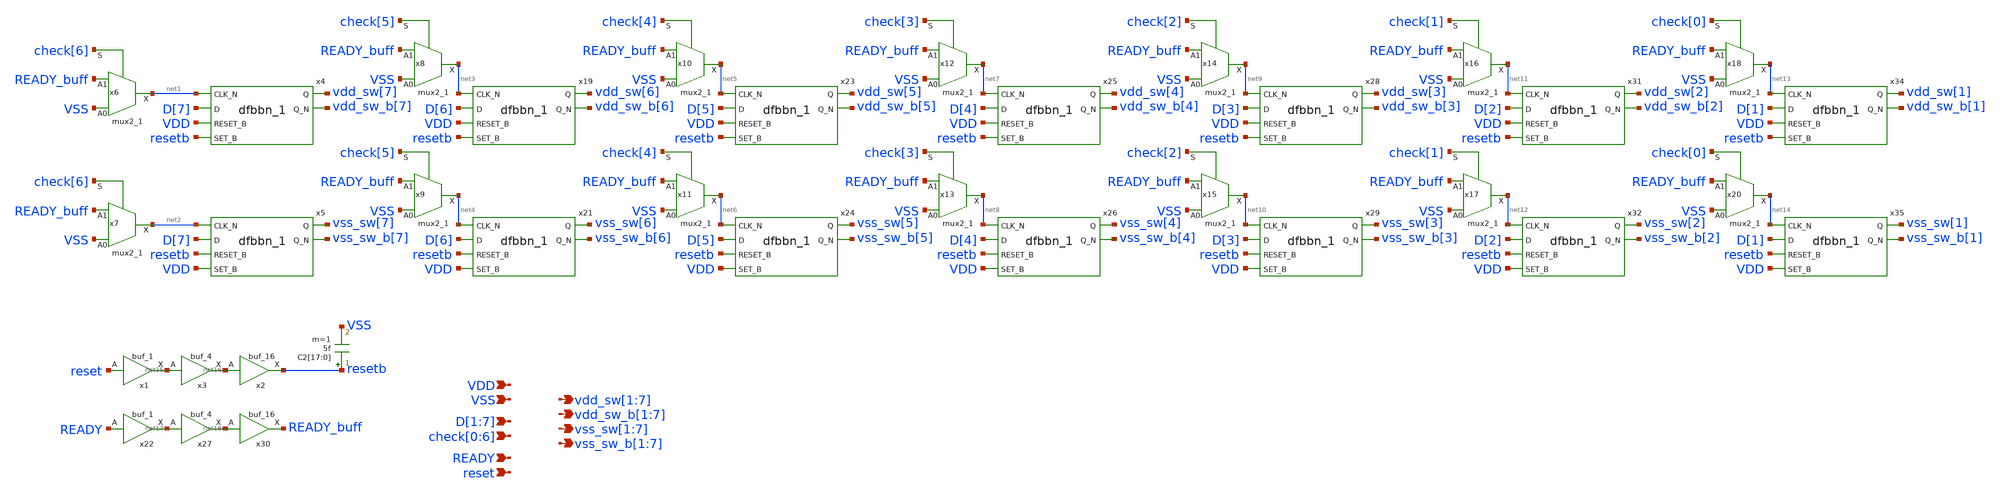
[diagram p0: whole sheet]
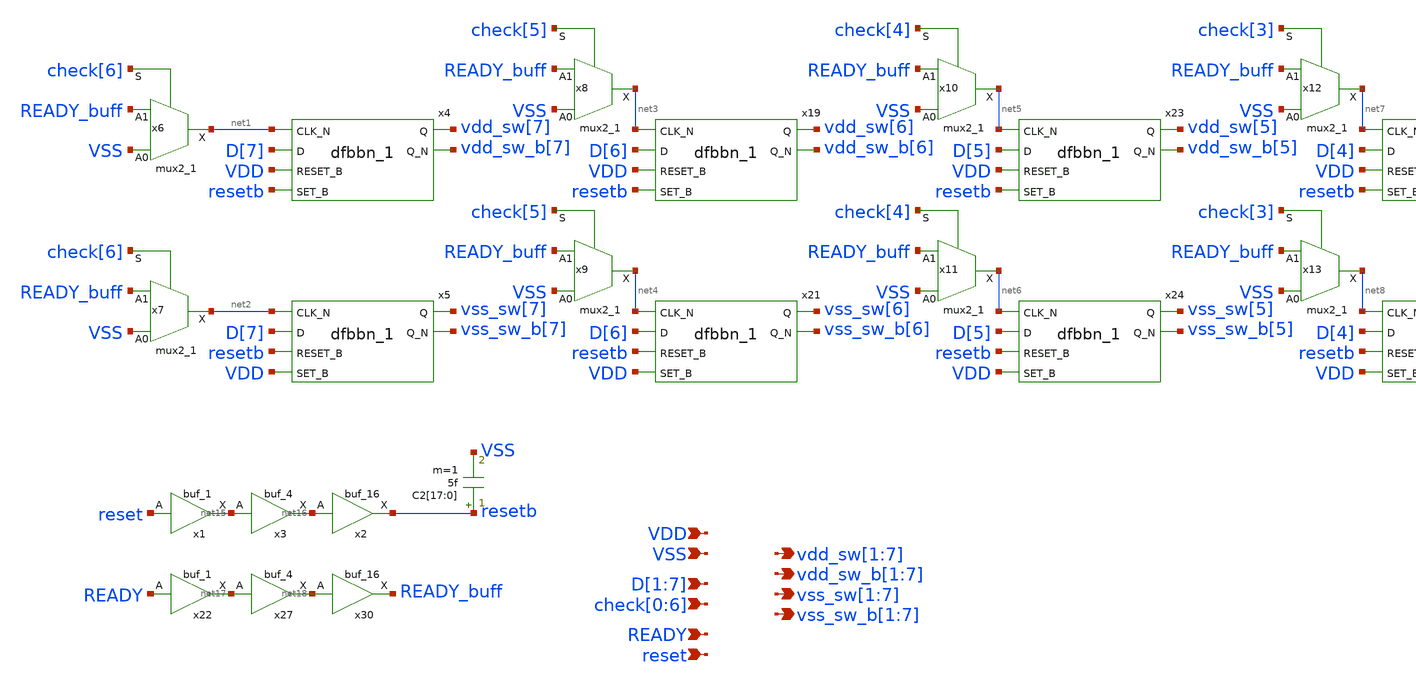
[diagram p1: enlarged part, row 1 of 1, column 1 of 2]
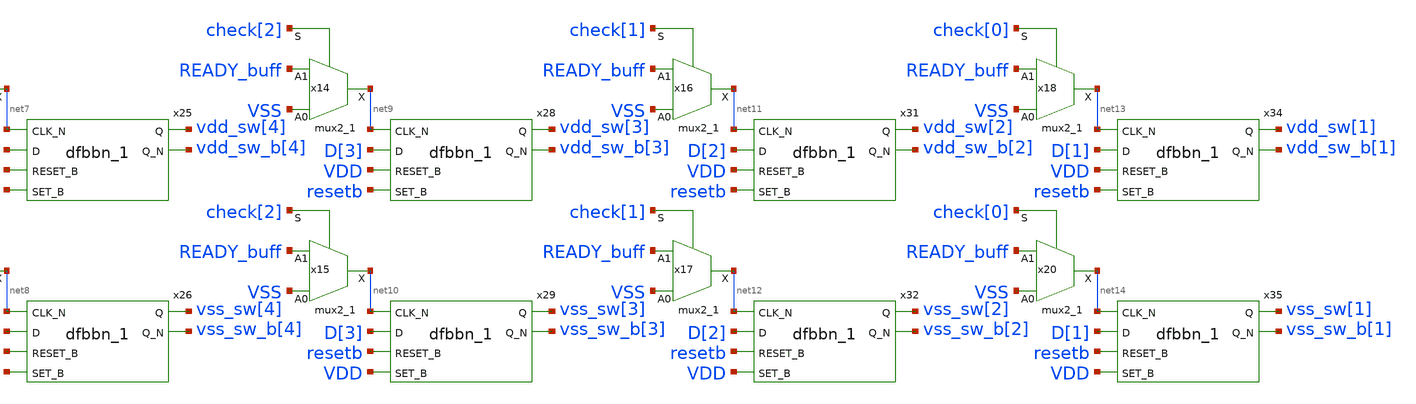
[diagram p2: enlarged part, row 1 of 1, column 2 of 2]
** sch_path: hgu/xschem/hgu_sarlogic_sw_ctrl.sch
**.subckt hgu_sarlogic_sw_ctrl vdd_sw[1],vdd_sw[2],vdd_sw[3],vdd_sw[4],vdd_sw[5],vdd_sw[6],vdd_sw[7]
*+ vdd_sw_b[1],vdd_sw_b[2],vdd_sw_b[3],vdd_sw_b[4],vdd_sw_b[5],vdd_sw_b[6],vdd_sw_b[7] vss_sw[1],vss_sw[2],vss_sw[3],vss_sw[4],vss_sw[5],vss_sw[6],vss_sw[7]
*+ vss_sw_b[1],vss_sw_b[2],vss_sw_b[3],vss_sw_b[4],vss_sw_b[5],vss_sw_b[6],vss_sw_b[7] VDD VSS READY D[1],D[2],D[3],D[4],D[5],D[6],D[7]
*+ check[0],check[1],check[2],check[3],check[4],check[5],check[6] reset
*.opin vdd_sw[1],vdd_sw[2],vdd_sw[3],vdd_sw[4],vdd_sw[5],vdd_sw[6],vdd_sw[7]
*.opin vdd_sw_b[1],vdd_sw_b[2],vdd_sw_b[3],vdd_sw_b[4],vdd_sw_b[5],vdd_sw_b[6],vdd_sw_b[7]
*.opin vss_sw[1],vss_sw[2],vss_sw[3],vss_sw[4],vss_sw[5],vss_sw[6],vss_sw[7]
*.opin vss_sw_b[1],vss_sw_b[2],vss_sw_b[3],vss_sw_b[4],vss_sw_b[5],vss_sw_b[6],vss_sw_b[7]
*.ipin VDD
*.ipin VSS
*.ipin READY
*.ipin D[1],D[2],D[3],D[4],D[5],D[6],D[7]
*.ipin check[0],check[1],check[2],check[3],check[4],check[5],check[6]
*.ipin reset
x4 net1 D[7] VDD resetb VSS VSS VDD VDD vdd_sw[7] vdd_sw_b[7] sky130_fd_sc_hd__dfbbn_1
x5 net2 D[7] resetb VDD VSS VSS VDD VDD vss_sw[7] vss_sw_b[7] sky130_fd_sc_hd__dfbbn_1
x19 net3 D[6] VDD resetb VSS VSS VDD VDD vdd_sw[6] vdd_sw_b[6] sky130_fd_sc_hd__dfbbn_1
x21 net4 D[6] resetb VDD VSS VSS VDD VDD vss_sw[6] vss_sw_b[6] sky130_fd_sc_hd__dfbbn_1
x23 net5 D[5] VDD resetb VSS VSS VDD VDD vdd_sw[5] vdd_sw_b[5] sky130_fd_sc_hd__dfbbn_1
x24 net6 D[5] resetb VDD VSS VSS VDD VDD vss_sw[5] vss_sw_b[5] sky130_fd_sc_hd__dfbbn_1
x25 net7 D[4] VDD resetb VSS VSS VDD VDD vdd_sw[4] vdd_sw_b[4] sky130_fd_sc_hd__dfbbn_1
x26 net8 D[4] resetb VDD VSS VSS VDD VDD vss_sw[4] vss_sw_b[4] sky130_fd_sc_hd__dfbbn_1
x28 net9 D[3] VDD resetb VSS VSS VDD VDD vdd_sw[3] vdd_sw_b[3] sky130_fd_sc_hd__dfbbn_1
x29 net10 D[3] resetb VDD VSS VSS VDD VDD vss_sw[3] vss_sw_b[3] sky130_fd_sc_hd__dfbbn_1
x31 net11 D[2] VDD resetb VSS VSS VDD VDD vdd_sw[2] vdd_sw_b[2] sky130_fd_sc_hd__dfbbn_1
x32 net12 D[2] resetb VDD VSS VSS VDD VDD vss_sw[2] vss_sw_b[2] sky130_fd_sc_hd__dfbbn_1
x34 net13 D[1] VDD resetb VSS VSS VDD VDD vdd_sw[1] vdd_sw_b[1] sky130_fd_sc_hd__dfbbn_1
x35 net14 D[1] resetb VDD VSS VSS VDD VDD vss_sw[1] vss_sw_b[1] sky130_fd_sc_hd__dfbbn_1
x6 VSS READY_buff check[6] VSS VSS VDD VDD net1 sky130_fd_sc_hd__mux2_1
x7 VSS READY_buff check[6] VSS VSS VDD VDD net2 sky130_fd_sc_hd__mux2_1
x8 VSS READY_buff check[5] VSS VSS VDD VDD net3 sky130_fd_sc_hd__mux2_1
x9 VSS READY_buff check[5] VSS VSS VDD VDD net4 sky130_fd_sc_hd__mux2_1
x10 VSS READY_buff check[4] VSS VSS VDD VDD net5 sky130_fd_sc_hd__mux2_1
x11 VSS READY_buff check[4] VSS VSS VDD VDD net6 sky130_fd_sc_hd__mux2_1
x12 VSS READY_buff check[3] VSS VSS VDD VDD net7 sky130_fd_sc_hd__mux2_1
x13 VSS READY_buff check[3] VSS VSS VDD VDD net8 sky130_fd_sc_hd__mux2_1
x14 VSS READY_buff check[2] VSS VSS VDD VDD net9 sky130_fd_sc_hd__mux2_1
x15 VSS READY_buff check[2] VSS VSS VDD VDD net10 sky130_fd_sc_hd__mux2_1
x16 VSS READY_buff check[1] VSS VSS VDD VDD net11 sky130_fd_sc_hd__mux2_1
x17 VSS READY_buff check[1] VSS VSS VDD VDD net12 sky130_fd_sc_hd__mux2_1
x18 VSS READY_buff check[0] VSS VSS VDD VDD net13 sky130_fd_sc_hd__mux2_1
x20 VSS READY_buff check[0] VSS VSS VDD VDD net14 sky130_fd_sc_hd__mux2_1
C2[17] resetb VSS 5f m=1
C2[16] resetb VSS 5f m=1
C2[15] resetb VSS 5f m=1
C2[14] resetb VSS 5f m=1
C2[13] resetb VSS 5f m=1
C2[12] resetb VSS 5f m=1
C2[11] resetb VSS 5f m=1
C2[10] resetb VSS 5f m=1
C2[9] resetb VSS 5f m=1
C2[8] resetb VSS 5f m=1
C2[7] resetb VSS 5f m=1
C2[6] resetb VSS 5f m=1
C2[5] resetb VSS 5f m=1
C2[4] resetb VSS 5f m=1
C2[3] resetb VSS 5f m=1
C2[2] resetb VSS 5f m=1
C2[1] resetb VSS 5f m=1
C2[0] resetb VSS 5f m=1
x1 reset VSS VSS VDD VDD net15 sky130_fd_sc_hd__buf_1
x3 net15 VSS VSS VDD VDD net16 sky130_fd_sc_hd__buf_4
x2 net16 VSS VSS VDD VDD resetb sky130_fd_sc_hd__buf_16
x22 READY VSS VSS VDD VDD net17 sky130_fd_sc_hd__buf_1
x27 net17 VSS VSS VDD VDD net18 sky130_fd_sc_hd__buf_4
x30 net18 VSS VSS VDD VDD READY_buff sky130_fd_sc_hd__buf_16
**** begin user architecture code



.lib /foss/pdks/sky130A/libs.tech/ngspice/sky130.lib.spice tt
.include /foss/pdks/sky130A/libs.ref/sky130_fd_sc_hd/spice/sky130_fd_sc_hd.spice
.include /foss/designs/hgu_goss/hgu/mag/hgu_cdac_unit.spice



**** end user architecture code
**.ends
.end
